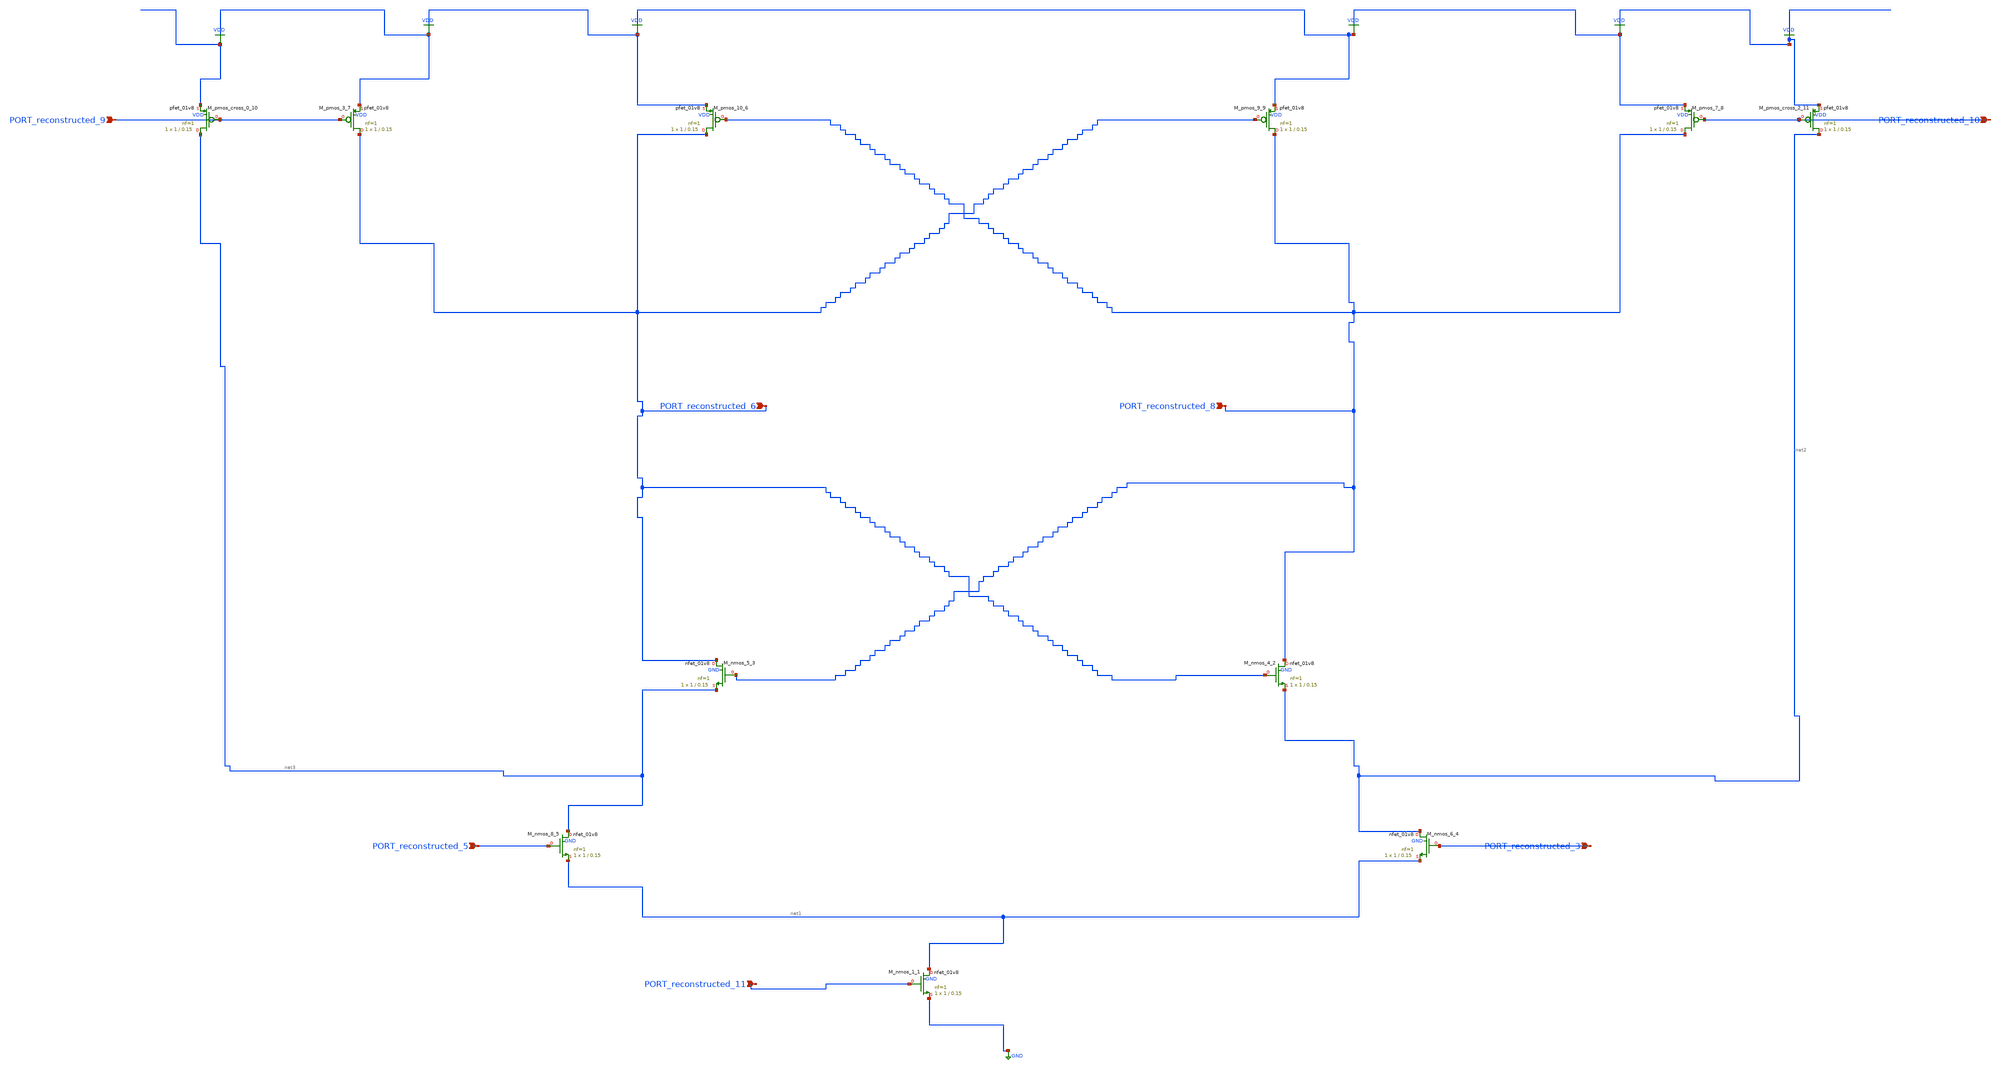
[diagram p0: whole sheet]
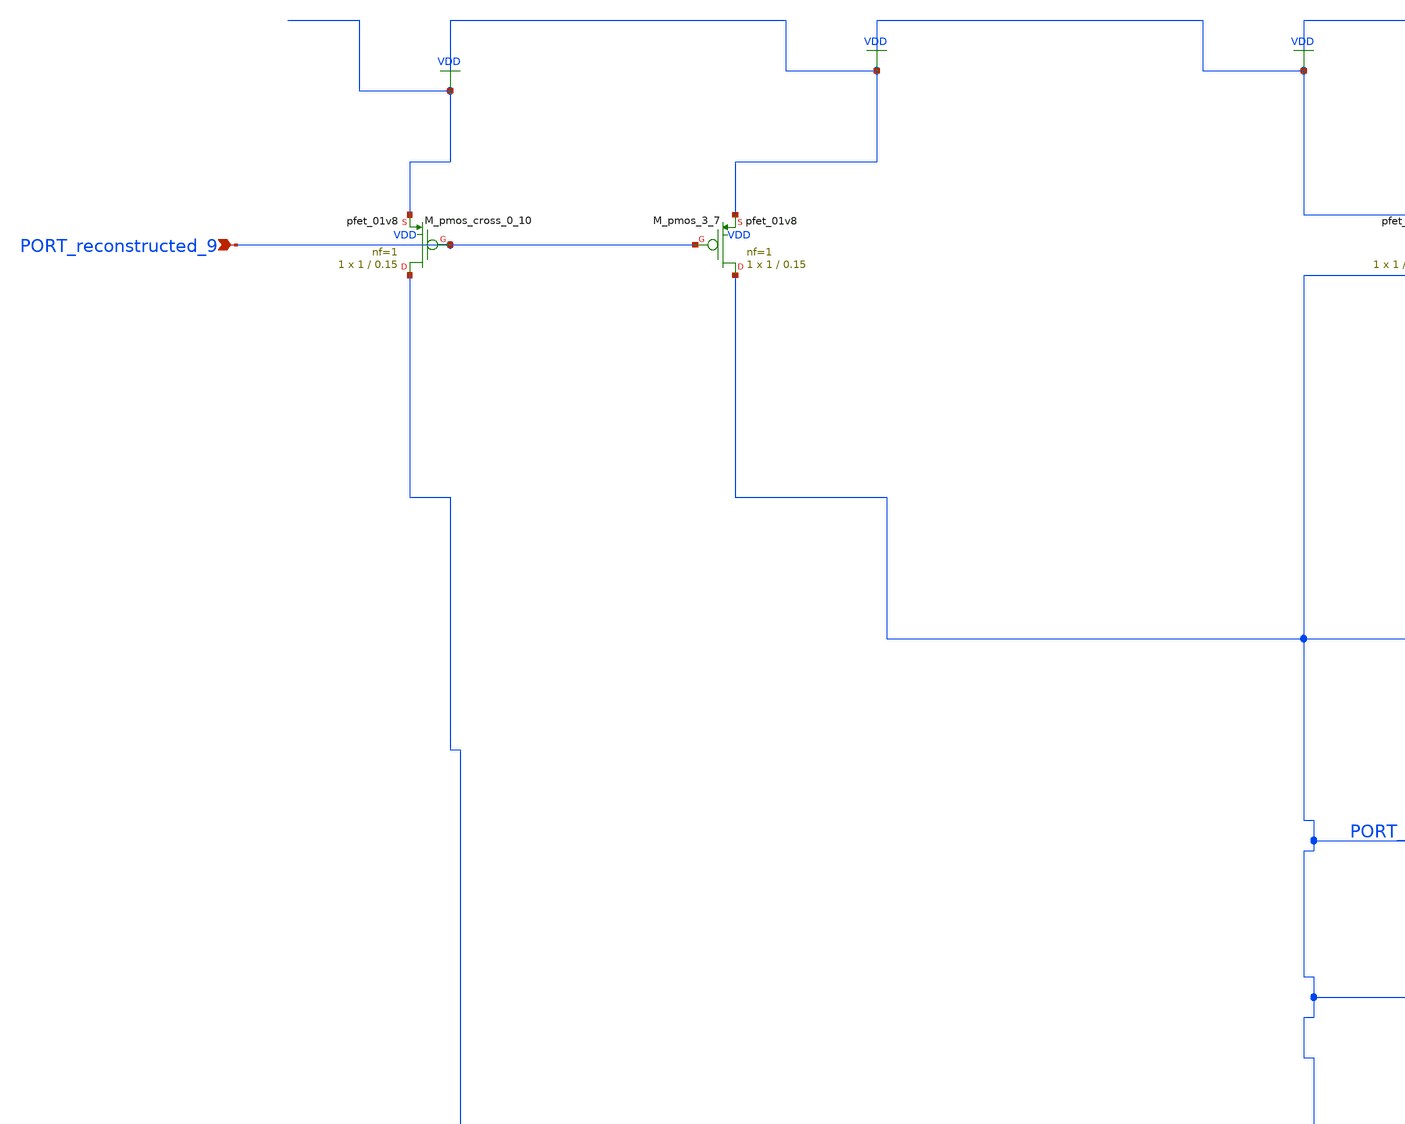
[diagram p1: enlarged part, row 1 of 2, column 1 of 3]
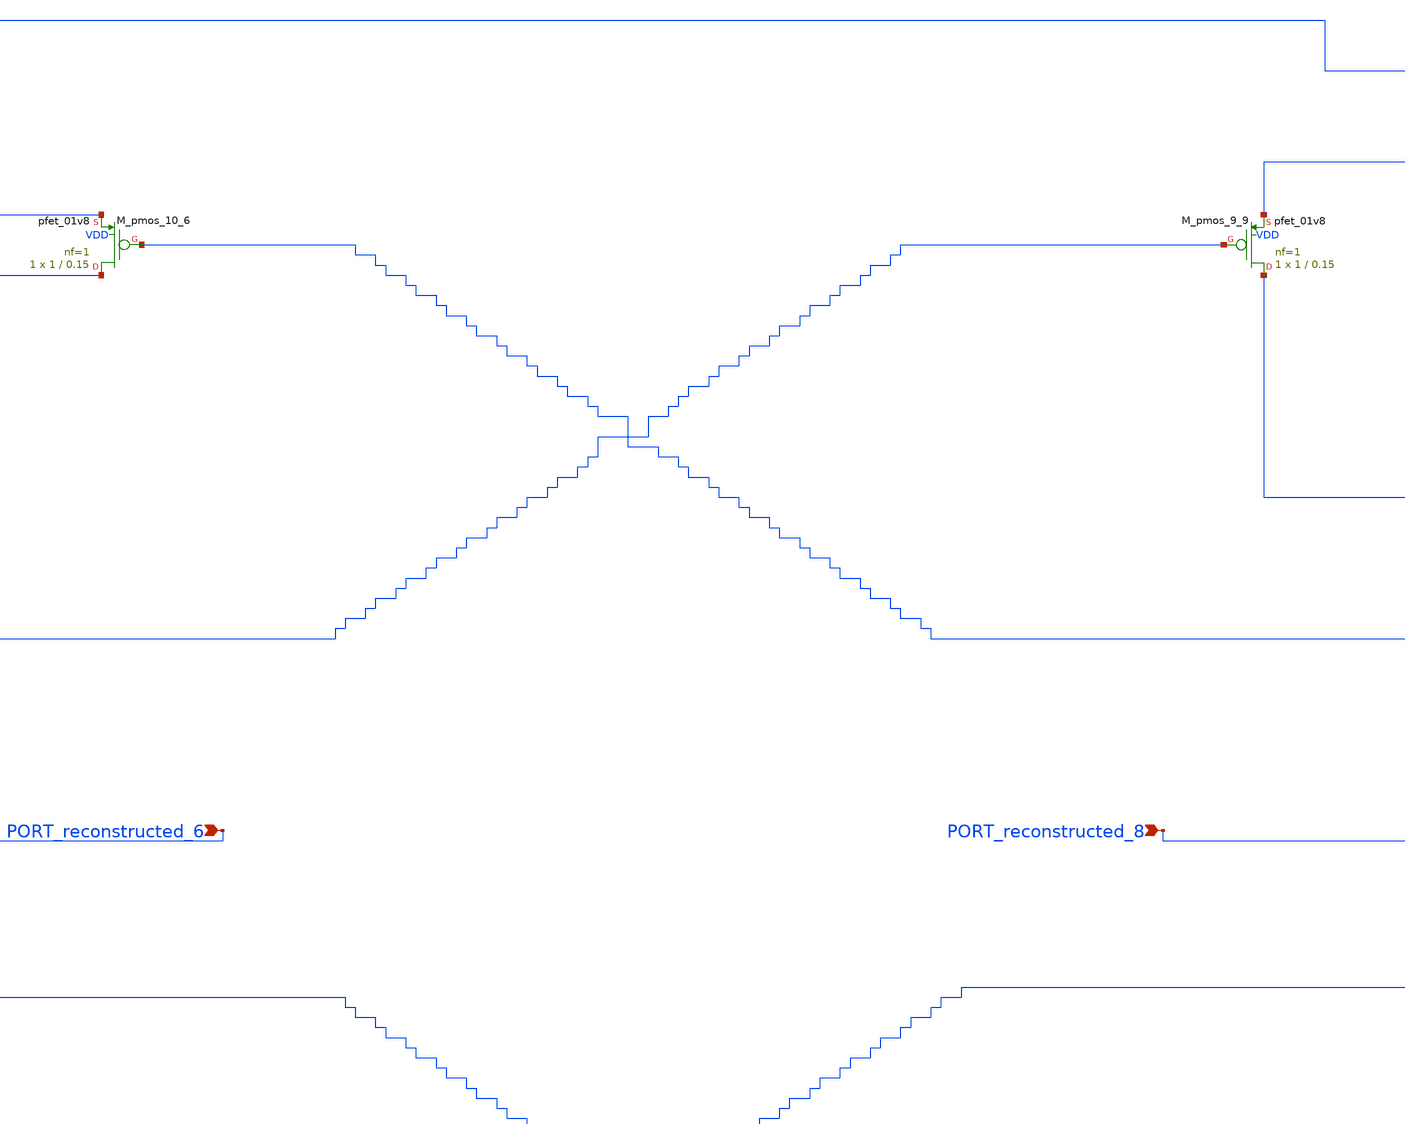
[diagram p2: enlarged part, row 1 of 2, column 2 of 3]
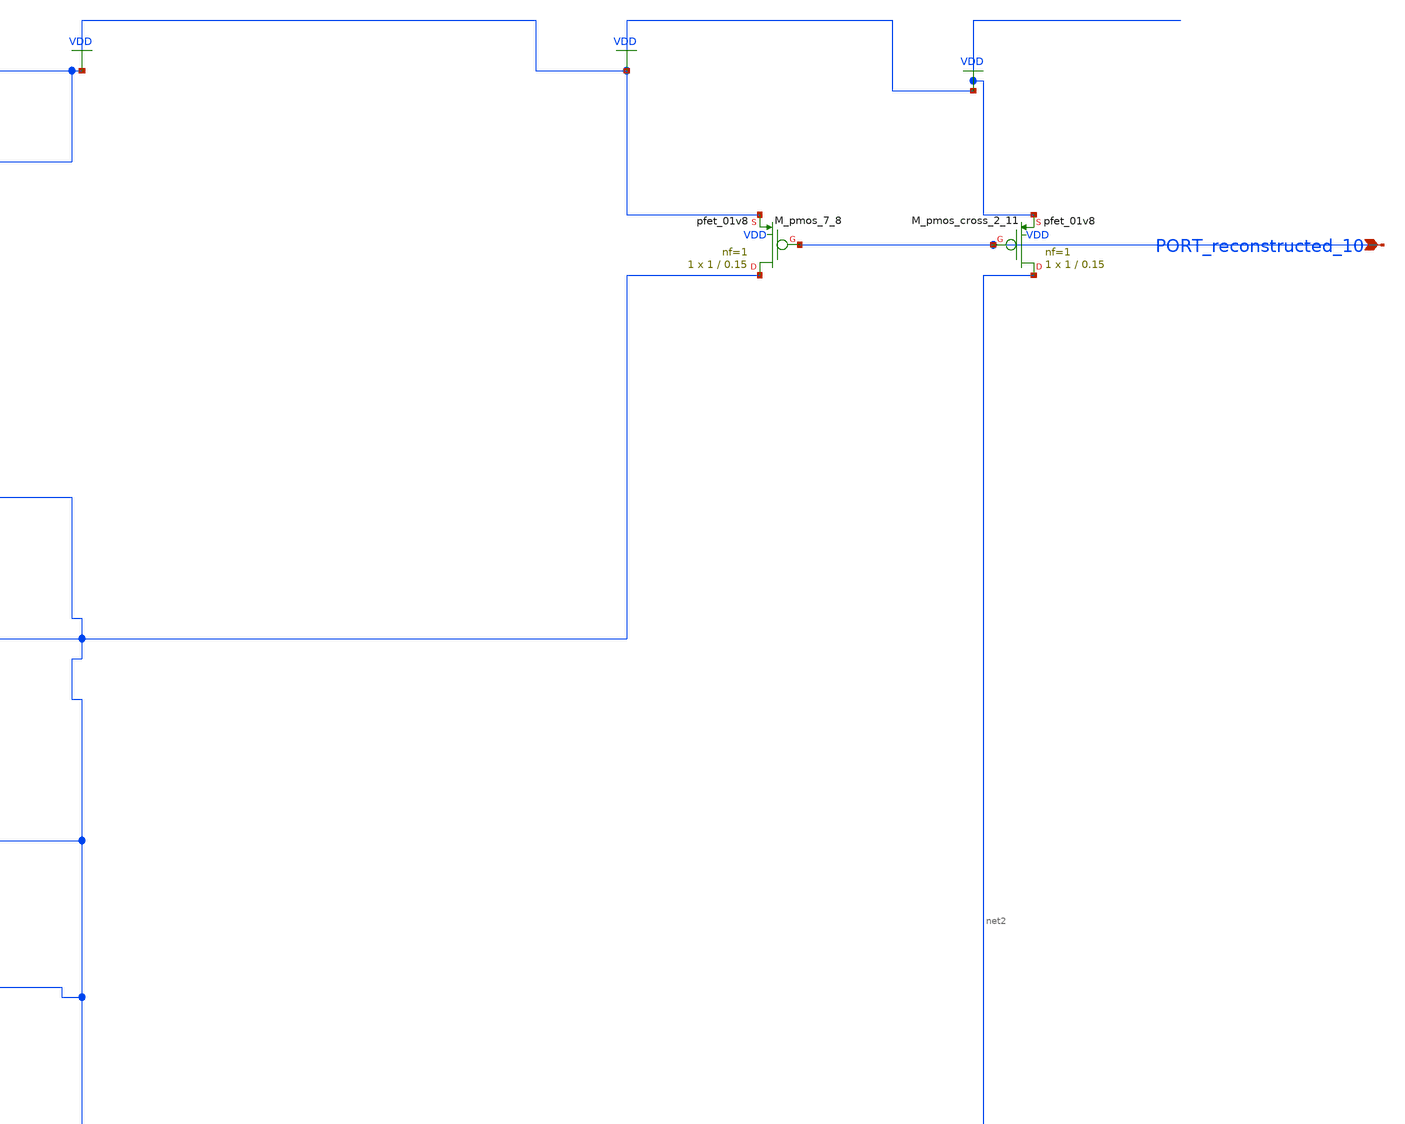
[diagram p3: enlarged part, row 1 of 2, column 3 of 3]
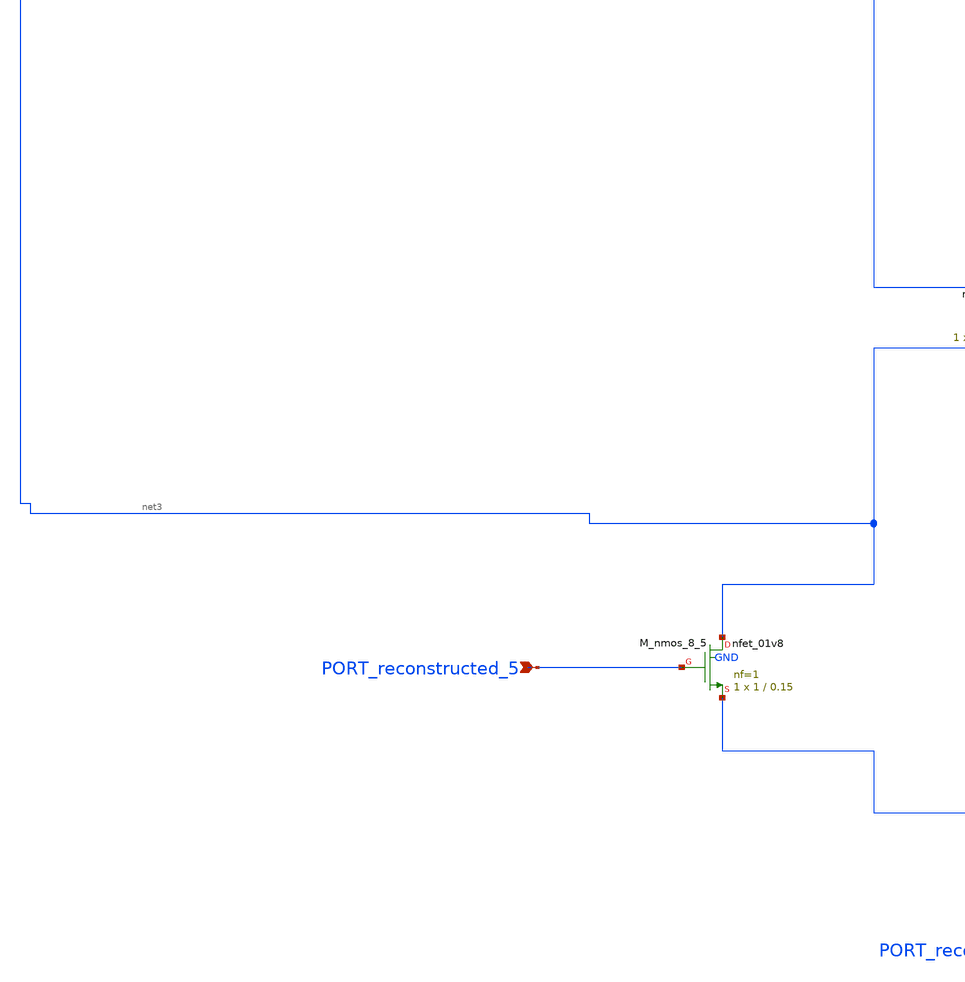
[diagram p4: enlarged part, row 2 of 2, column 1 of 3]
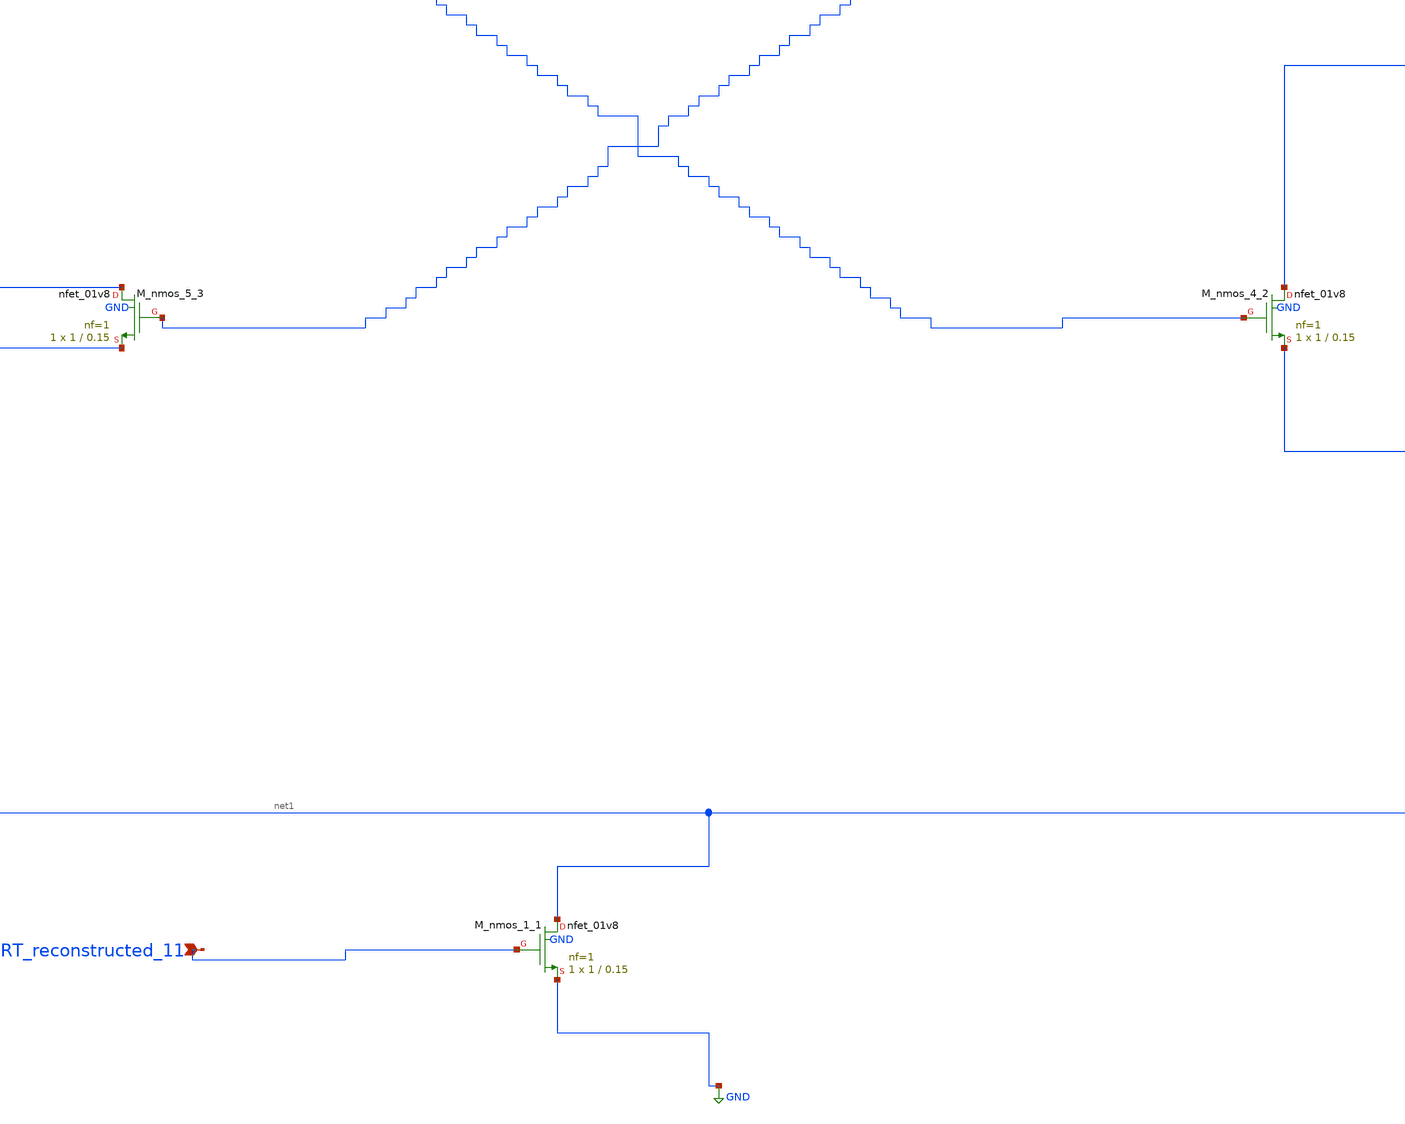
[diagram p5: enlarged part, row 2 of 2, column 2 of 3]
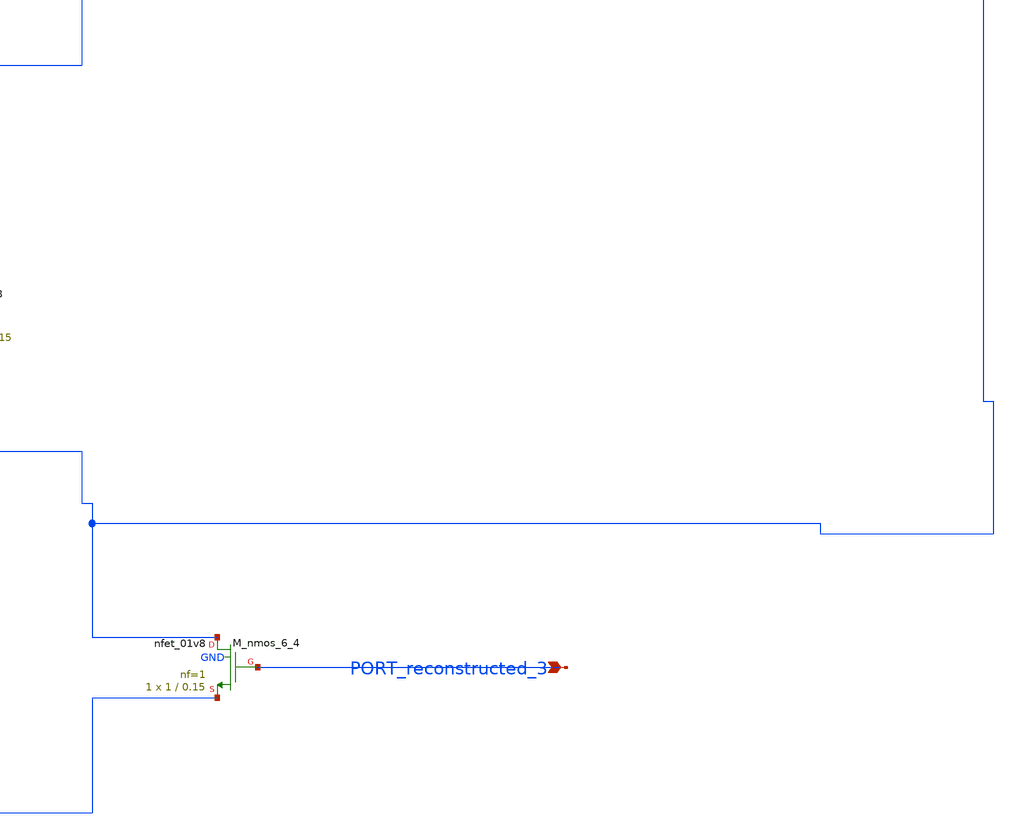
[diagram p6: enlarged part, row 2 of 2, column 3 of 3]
** sch_path: schematics/Image2Net/099.sch
**.subckt 099 PORT_reconstructed_3 PORT_reconstructed_5 PORT_reconstructed_10 PORT_reconstructed_11
*+ PORT_reconstructed_9 PORT_reconstructed_6 PORT_reconstructed_8
*.ipin PORT_reconstructed_3
*.ipin PORT_reconstructed_5
*.ipin PORT_reconstructed_10
*.ipin PORT_reconstructed_11
*.ipin PORT_reconstructed_9
*.ipin PORT_reconstructed_6
*.ipin PORT_reconstructed_8
XM_nmos_1_1 net1 PORT_reconstructed_11 GND GND sky130_fd_pr__nfet_01v8 L=0.15 W=1 nf=1 ad='int((1 + 1)/2) * 1 / 1 * 0.29'
+ as='int((1 + 2)/2) * 1 / 1 * 0.29' pd='2*int((1 + 1)/2) * (1 / 1 + 0.29)' ps='2*int((1 + 2)/2) * (1 / 1 + 0.29)'
+ nrd='0.29 / 1 ' nrs='0.29 / 1 ' sa=0 sb=0 sd=0 mult=1 m=1
XM_nmos_4_2 PORT_reconstructed_8 PORT_reconstructed_6 net2 GND sky130_fd_pr__nfet_01v8 L=0.15 W=1 nf=1
+ ad='int((1 + 1)/2) * 1 / 1 * 0.29' as='int((1 + 2)/2) * 1 / 1 * 0.29' pd='2*int((1 + 1)/2) * (1 / 1 + 0.29)'
+ ps='2*int((1 + 2)/2) * (1 / 1 + 0.29)' nrd='0.29 / 1 ' nrs='0.29 / 1 ' sa=0 sb=0 sd=0 mult=1 m=1
XM_nmos_5_3 PORT_reconstructed_6 PORT_reconstructed_8 net3 GND sky130_fd_pr__nfet_01v8 L=0.15 W=1 nf=1
+ ad='int((1 + 1)/2) * 1 / 1 * 0.29' as='int((1 + 2)/2) * 1 / 1 * 0.29' pd='2*int((1 + 1)/2) * (1 / 1 + 0.29)'
+ ps='2*int((1 + 2)/2) * (1 / 1 + 0.29)' nrd='0.29 / 1 ' nrs='0.29 / 1 ' sa=0 sb=0 sd=0 mult=1 m=1
XM_nmos_6_4 net2 PORT_reconstructed_3 net1 GND sky130_fd_pr__nfet_01v8 L=0.15 W=1 nf=1 ad='int((1 + 1)/2) * 1 / 1 * 0.29'
+ as='int((1 + 2)/2) * 1 / 1 * 0.29' pd='2*int((1 + 1)/2) * (1 / 1 + 0.29)' ps='2*int((1 + 2)/2) * (1 / 1 + 0.29)'
+ nrd='0.29 / 1 ' nrs='0.29 / 1 ' sa=0 sb=0 sd=0 mult=1 m=1
XM_nmos_8_5 net3 PORT_reconstructed_5 net1 GND sky130_fd_pr__nfet_01v8 L=0.15 W=1 nf=1 ad='int((1 + 1)/2) * 1 / 1 * 0.29'
+ as='int((1 + 2)/2) * 1 / 1 * 0.29' pd='2*int((1 + 1)/2) * (1 / 1 + 0.29)' ps='2*int((1 + 2)/2) * (1 / 1 + 0.29)'
+ nrd='0.29 / 1 ' nrs='0.29 / 1 ' sa=0 sb=0 sd=0 mult=1 m=1
XM_pmos_10_6 PORT_reconstructed_6 PORT_reconstructed_8 VDD VDD sky130_fd_pr__pfet_01v8 L=0.15 W=1 nf=1
+ ad='int((1 + 1)/2) * 1 / 1 * 0.29' as='int((1 + 2)/2) * 1 / 1 * 0.29' pd='2*int((1 + 1)/2) * (1 / 1 + 0.29)'
+ ps='2*int((1 + 2)/2) * (1 / 1 + 0.29)' nrd='0.29 / 1 ' nrs='0.29 / 1 ' sa=0 sb=0 sd=0 mult=1 m=1
XM_pmos_3_7 PORT_reconstructed_6 PORT_reconstructed_9 VDD VDD sky130_fd_pr__pfet_01v8 L=0.15 W=1 nf=1
+ ad='int((1 + 1)/2) * 1 / 1 * 0.29' as='int((1 + 2)/2) * 1 / 1 * 0.29' pd='2*int((1 + 1)/2) * (1 / 1 + 0.29)'
+ ps='2*int((1 + 2)/2) * (1 / 1 + 0.29)' nrd='0.29 / 1 ' nrs='0.29 / 1 ' sa=0 sb=0 sd=0 mult=1 m=1
XM_pmos_7_8 PORT_reconstructed_8 PORT_reconstructed_10 VDD VDD sky130_fd_pr__pfet_01v8 L=0.15 W=1 nf=1
+ ad='int((1 + 1)/2) * 1 / 1 * 0.29' as='int((1 + 2)/2) * 1 / 1 * 0.29' pd='2*int((1 + 1)/2) * (1 / 1 + 0.29)'
+ ps='2*int((1 + 2)/2) * (1 / 1 + 0.29)' nrd='0.29 / 1 ' nrs='0.29 / 1 ' sa=0 sb=0 sd=0 mult=1 m=1
XM_pmos_9_9 PORT_reconstructed_8 PORT_reconstructed_6 VDD VDD sky130_fd_pr__pfet_01v8 L=0.15 W=1 nf=1
+ ad='int((1 + 1)/2) * 1 / 1 * 0.29' as='int((1 + 2)/2) * 1 / 1 * 0.29' pd='2*int((1 + 1)/2) * (1 / 1 + 0.29)'
+ ps='2*int((1 + 2)/2) * (1 / 1 + 0.29)' nrd='0.29 / 1 ' nrs='0.29 / 1 ' sa=0 sb=0 sd=0 mult=1 m=1
XM_pmos_cross_0_10 net3 PORT_reconstructed_9 VDD VDD sky130_fd_pr__pfet_01v8 L=0.15 W=1 nf=1 ad='int((1 + 1)/2) * 1 / 1 * 0.29'
+ as='int((1 + 2)/2) * 1 / 1 * 0.29' pd='2*int((1 + 1)/2) * (1 / 1 + 0.29)' ps='2*int((1 + 2)/2) * (1 / 1 + 0.29)'
+ nrd='0.29 / 1 ' nrs='0.29 / 1 ' sa=0 sb=0 sd=0 mult=1 m=1
XM_pmos_cross_2_11 net2 PORT_reconstructed_10 VDD VDD sky130_fd_pr__pfet_01v8 L=0.15 W=1 nf=1 ad='int((1 + 1)/2) * 1 / 1 * 0.29'
+ as='int((1 + 2)/2) * 1 / 1 * 0.29' pd='2*int((1 + 1)/2) * (1 / 1 + 0.29)' ps='2*int((1 + 2)/2) * (1 / 1 + 0.29)'
+ nrd='0.29 / 1 ' nrs='0.29 / 1 ' sa=0 sb=0 sd=0 mult=1 m=1
**.ends
.GLOBAL GND
.GLOBAL VDD
.end
